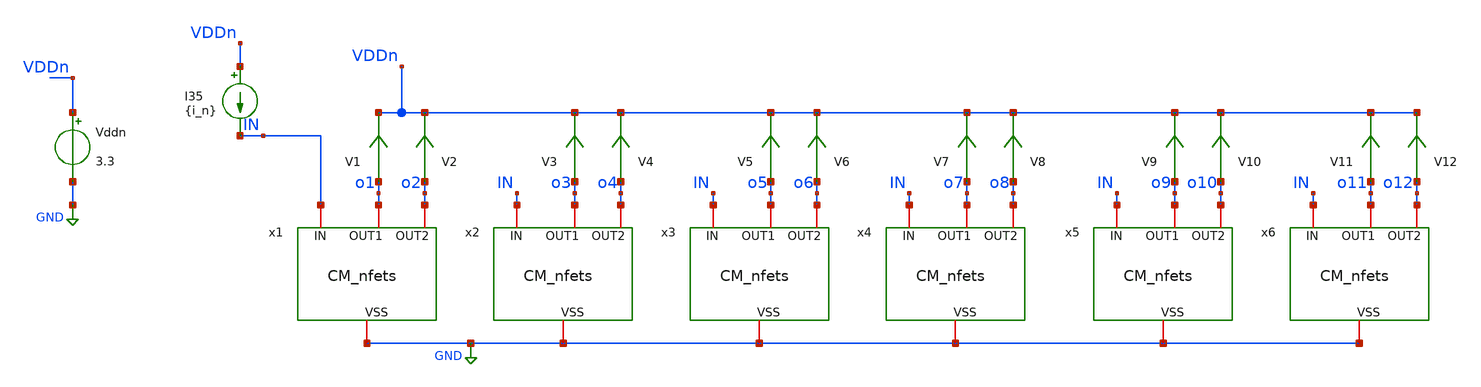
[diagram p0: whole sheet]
** sch_path: TIA_Filter/CurrentMirrors/TB_CM.sch
**.subckt TB_CM
I35 VDDn IN {i_n}
Vddn VDDn GND 3.3
V1 o1 VDDn 0
.save i(v1)
V2 o2 VDDn 0
.save i(v2)
V3 o3 VDDn 0
.save i(v3)
V4 o4 VDDn 0
.save i(v4)
V5 o5 VDDn 0
.save i(v5)
V6 o6 VDDn 0
.save i(v6)
V7 o7 VDDn 0
.save i(v7)
V8 o8 VDDn 0
.save i(v8)
V9 o9 VDDn 0
.save i(v9)
V10 o10 VDDn 0
.save i(v10)
V11 o11 VDDn 0
.save i(v11)
V12 o12 VDDn 0
.save i(v12)
x1 IN o1 o2 GND CM_nfets
x2 IN o3 o4 GND CM_nfets
x3 IN o5 o6 GND CM_nfets
x4 IN o7 o8 GND CM_nfets
x5 IN o9 o10 GND CM_nfets
x6 IN o11 o12 GND CM_nfets
**** begin user architecture code

.include $::180MCU_MODELS/design.ngspice
.lib $::180MCU_MODELS/sm141064.ngspice typical
*.param sw_stat_mismatch=1
*.param sw_stat_global=1

*.include /home/gmaranhao/Desktop/Bracolin/TIA_Filter/CurrentMirrors/layout/spice/CM_nfets_pex4.spice

*.subckt CM_nfets VSS OUT1 OUT2 IN

*Xdut 0 o1 o2 IN CM_nfets
*Xdut2 0 o3 o4 IN CM_nfets
*Xdut3 0 o5 o6 IN CM_nfets
*Xdut4 0 o7 o8 IN CM_nfets
*Xdut5 0 o9 o10 IN CM_nfets
*Xdut6 0 o11 o12 IN CM_nfets




.option gmin=1e-26
.option abstol=1e-18
.option retol=1e-15

.param i_n=1n

.control
save all

let sample_num = 0

*while sample_num<151

reset
op
remzerovec
write TB_CM.raw
*wrdata /home/gmaranhao/Desktop/Bracolin/TIA_Filter/CurrentMirrors/out_cm.txt i(V1) i(V2) i(V3)
*+ i(V4) i(V5) i(V6) i(V7) i(V8) i(V9) i(V
10) i(V11) i(V12)
set appendwrite

*let sample_num = sample_num + 1
*end


.endc
.save all


**** end user architecture code
**.ends

* expanding   symbol:  CurrentMirrors/CM_nfets.sym # of pins=4
** sym_path: TIA_Filter/CurrentMirrors/CM_nfets.sym
** sch_path: TIA_Filter/CurrentMirrors/CM_nfets.sch
.subckt CM_nfets IN OUT1 OUT2 VSS
*.iopin IN
*.iopin OUT1
*.iopin OUT2
*.iopin VSS
XM2[1] IN IN VSS VSS nfet_03v3 L=2u W=2u nf=1 ad='int((nf+1)/2) * W/nf * 0.18u' as='int((nf+2)/2) * W/nf * 0.18u'
+ pd='2*int((nf+1)/2) * (W/nf + 0.18u)' ps='2*int((nf+2)/2) * (W/nf + 0.18u)' nrd='0.18u / W' nrs='0.18u / W'
+ sa=0 sb=0 sd=0 m=1
XM2[2] IN IN VSS VSS nfet_03v3 L=2u W=2u nf=1 ad='int((nf+1)/2) * W/nf * 0.18u' as='int((nf+2)/2) * W/nf * 0.18u'
+ pd='2*int((nf+1)/2) * (W/nf + 0.18u)' ps='2*int((nf+2)/2) * (W/nf + 0.18u)' nrd='0.18u / W' nrs='0.18u / W'
+ sa=0 sb=0 sd=0 m=1
XM2[3] IN IN VSS VSS nfet_03v3 L=2u W=2u nf=1 ad='int((nf+1)/2) * W/nf * 0.18u' as='int((nf+2)/2) * W/nf * 0.18u'
+ pd='2*int((nf+1)/2) * (W/nf + 0.18u)' ps='2*int((nf+2)/2) * (W/nf + 0.18u)' nrd='0.18u / W' nrs='0.18u / W'
+ sa=0 sb=0 sd=0 m=1
XM2[4] IN IN VSS VSS nfet_03v3 L=2u W=2u nf=1 ad='int((nf+1)/2) * W/nf * 0.18u' as='int((nf+2)/2) * W/nf * 0.18u'
+ pd='2*int((nf+1)/2) * (W/nf + 0.18u)' ps='2*int((nf+2)/2) * (W/nf + 0.18u)' nrd='0.18u / W' nrs='0.18u / W'
+ sa=0 sb=0 sd=0 m=1
XM2[5] IN IN VSS VSS nfet_03v3 L=2u W=2u nf=1 ad='int((nf+1)/2) * W/nf * 0.18u' as='int((nf+2)/2) * W/nf * 0.18u'
+ pd='2*int((nf+1)/2) * (W/nf + 0.18u)' ps='2*int((nf+2)/2) * (W/nf + 0.18u)' nrd='0.18u / W' nrs='0.18u / W'
+ sa=0 sb=0 sd=0 m=1
XM2[6] IN IN VSS VSS nfet_03v3 L=2u W=2u nf=1 ad='int((nf+1)/2) * W/nf * 0.18u' as='int((nf+2)/2) * W/nf * 0.18u'
+ pd='2*int((nf+1)/2) * (W/nf + 0.18u)' ps='2*int((nf+2)/2) * (W/nf + 0.18u)' nrd='0.18u / W' nrs='0.18u / W'
+ sa=0 sb=0 sd=0 m=1
XM2 OUT1 IN net3 VSS nfet_03v3 L=2u W=2u nf=1 ad='int((nf+1)/2) * W/nf * 0.18u' as='int((nf+2)/2) * W/nf * 0.18u'
+ pd='2*int((nf+1)/2) * (W/nf + 0.18u)' ps='2*int((nf+2)/2) * (W/nf + 0.18u)' nrd='0.18u / W' nrs='0.18u / W'
+ sa=0 sb=0 sd=0 m=1
XM11 net4 IN net6 VSS nfet_03v3 L=2u W=2u nf=1 ad='int((nf+1)/2) * W/nf * 0.18u' as='int((nf+2)/2) * W/nf * 0.18u'
+ pd='2*int((nf+1)/2) * (W/nf + 0.18u)' ps='2*int((nf+2)/2) * (W/nf + 0.18u)' nrd='0.18u / W' nrs='0.18u / W'
+ sa=0 sb=0 sd=0 m=1
XM12 net6 IN net7 VSS nfet_03v3 L=2u W=2u nf=1 ad='int((nf+1)/2) * W/nf * 0.18u' as='int((nf+2)/2) * W/nf * 0.18u'
+ pd='2*int((nf+1)/2) * (W/nf + 0.18u)' ps='2*int((nf+2)/2) * (W/nf + 0.18u)' nrd='0.18u / W' nrs='0.18u / W'
+ sa=0 sb=0 sd=0 m=1
XM13 net7 IN net8 VSS nfet_03v3 L=2u W=2u nf=1 ad='int((nf+1)/2) * W/nf * 0.18u' as='int((nf+2)/2) * W/nf * 0.18u'
+ pd='2*int((nf+1)/2) * (W/nf + 0.18u)' ps='2*int((nf+2)/2) * (W/nf + 0.18u)' nrd='0.18u / W' nrs='0.18u / W'
+ sa=0 sb=0 sd=0 m=1
XM14 net8 IN net9 VSS nfet_03v3 L=2u W=2u nf=1 ad='int((nf+1)/2) * W/nf * 0.18u' as='int((nf+2)/2) * W/nf * 0.18u'
+ pd='2*int((nf+1)/2) * (W/nf + 0.18u)' ps='2*int((nf+2)/2) * (W/nf + 0.18u)' nrd='0.18u / W' nrs='0.18u / W'
+ sa=0 sb=0 sd=0 m=1
XM15 net9 IN net10 VSS nfet_03v3 L=2u W=2u nf=1 ad='int((nf+1)/2) * W/nf * 0.18u' as='int((nf+2)/2) * W/nf * 0.18u'
+ pd='2*int((nf+1)/2) * (W/nf + 0.18u)' ps='2*int((nf+2)/2) * (W/nf + 0.18u)' nrd='0.18u / W' nrs='0.18u / W'
+ sa=0 sb=0 sd=0 m=1
XM16 net10 IN net11 VSS nfet_03v3 L=2u W=2u nf=1 ad='int((nf+1)/2) * W/nf * 0.18u' as='int((nf+2)/2) * W/nf * 0.18u'
+ pd='2*int((nf+1)/2) * (W/nf + 0.18u)' ps='2*int((nf+2)/2) * (W/nf + 0.18u)' nrd='0.18u / W' nrs='0.18u / W'
+ sa=0 sb=0 sd=0 m=1
XM17 net11 IN net12 VSS nfet_03v3 L=2u W=2u nf=1 ad='int((nf+1)/2) * W/nf * 0.18u' as='int((nf+2)/2) * W/nf * 0.18u'
+ pd='2*int((nf+1)/2) * (W/nf + 0.18u)' ps='2*int((nf+2)/2) * (W/nf + 0.18u)' nrd='0.18u / W' nrs='0.18u / W'
+ sa=0 sb=0 sd=0 m=1
XM18 net12 IN net13 VSS nfet_03v3 L=2u W=2u nf=1 ad='int((nf+1)/2) * W/nf * 0.18u' as='int((nf+2)/2) * W/nf * 0.18u'
+ pd='2*int((nf+1)/2) * (W/nf + 0.18u)' ps='2*int((nf+2)/2) * (W/nf + 0.18u)' nrd='0.18u / W' nrs='0.18u / W'
+ sa=0 sb=0 sd=0 m=1
XM19 net13 IN net14 VSS nfet_03v3 L=2u W=2u nf=1 ad='int((nf+1)/2) * W/nf * 0.18u' as='int((nf+2)/2) * W/nf * 0.18u'
+ pd='2*int((nf+1)/2) * (W/nf + 0.18u)' ps='2*int((nf+2)/2) * (W/nf + 0.18u)' nrd='0.18u / W' nrs='0.18u / W'
+ sa=0 sb=0 sd=0 m=1
XM20 net14 IN net1 VSS nfet_03v3 L=2u W=2u nf=1 ad='int((nf+1)/2) * W/nf * 0.18u' as='int((nf+2)/2) * W/nf * 0.18u'
+ pd='2*int((nf+1)/2) * (W/nf + 0.18u)' ps='2*int((nf+2)/2) * (W/nf + 0.18u)' nrd='0.18u / W' nrs='0.18u / W'
+ sa=0 sb=0 sd=0 m=1
XM21 net1 IN net15 VSS nfet_03v3 L=2u W=2u nf=1 ad='int((nf+1)/2) * W/nf * 0.18u' as='int((nf+2)/2) * W/nf * 0.18u'
+ pd='2*int((nf+1)/2) * (W/nf + 0.18u)' ps='2*int((nf+2)/2) * (W/nf + 0.18u)' nrd='0.18u / W' nrs='0.18u / W'
+ sa=0 sb=0 sd=0 m=1
XM22 net15 IN net16 VSS nfet_03v3 L=2u W=2u nf=1 ad='int((nf+1)/2) * W/nf * 0.18u' as='int((nf+2)/2) * W/nf * 0.18u'
+ pd='2*int((nf+1)/2) * (W/nf + 0.18u)' ps='2*int((nf+2)/2) * (W/nf + 0.18u)' nrd='0.18u / W' nrs='0.18u / W'
+ sa=0 sb=0 sd=0 m=1
XM23 net16 IN net17 VSS nfet_03v3 L=2u W=2u nf=1 ad='int((nf+1)/2) * W/nf * 0.18u' as='int((nf+2)/2) * W/nf * 0.18u'
+ pd='2*int((nf+1)/2) * (W/nf + 0.18u)' ps='2*int((nf+2)/2) * (W/nf + 0.18u)' nrd='0.18u / W' nrs='0.18u / W'
+ sa=0 sb=0 sd=0 m=1
XM24 net17 IN net18 VSS nfet_03v3 L=2u W=2u nf=1 ad='int((nf+1)/2) * W/nf * 0.18u' as='int((nf+2)/2) * W/nf * 0.18u'
+ pd='2*int((nf+1)/2) * (W/nf + 0.18u)' ps='2*int((nf+2)/2) * (W/nf + 0.18u)' nrd='0.18u / W' nrs='0.18u / W'
+ sa=0 sb=0 sd=0 m=1
XM25 net18 IN net19 VSS nfet_03v3 L=2u W=2u nf=1 ad='int((nf+1)/2) * W/nf * 0.18u' as='int((nf+2)/2) * W/nf * 0.18u'
+ pd='2*int((nf+1)/2) * (W/nf + 0.18u)' ps='2*int((nf+2)/2) * (W/nf + 0.18u)' nrd='0.18u / W' nrs='0.18u / W'
+ sa=0 sb=0 sd=0 m=1
XM26 net19 IN net20 VSS nfet_03v3 L=2u W=2u nf=1 ad='int((nf+1)/2) * W/nf * 0.18u' as='int((nf+2)/2) * W/nf * 0.18u'
+ pd='2*int((nf+1)/2) * (W/nf + 0.18u)' ps='2*int((nf+2)/2) * (W/nf + 0.18u)' nrd='0.18u / W' nrs='0.18u / W'
+ sa=0 sb=0 sd=0 m=1
XM27 net20 IN net21 VSS nfet_03v3 L=2u W=2u nf=1 ad='int((nf+1)/2) * W/nf * 0.18u' as='int((nf+2)/2) * W/nf * 0.18u'
+ pd='2*int((nf+1)/2) * (W/nf + 0.18u)' ps='2*int((nf+2)/2) * (W/nf + 0.18u)' nrd='0.18u / W' nrs='0.18u / W'
+ sa=0 sb=0 sd=0 m=1
XM28 net21 IN net22 VSS nfet_03v3 L=2u W=2u nf=1 ad='int((nf+1)/2) * W/nf * 0.18u' as='int((nf+2)/2) * W/nf * 0.18u'
+ pd='2*int((nf+1)/2) * (W/nf + 0.18u)' ps='2*int((nf+2)/2) * (W/nf + 0.18u)' nrd='0.18u / W' nrs='0.18u / W'
+ sa=0 sb=0 sd=0 m=1
XM29 net22 IN net23 VSS nfet_03v3 L=2u W=2u nf=1 ad='int((nf+1)/2) * W/nf * 0.18u' as='int((nf+2)/2) * W/nf * 0.18u'
+ pd='2*int((nf+1)/2) * (W/nf + 0.18u)' ps='2*int((nf+2)/2) * (W/nf + 0.18u)' nrd='0.18u / W' nrs='0.18u / W'
+ sa=0 sb=0 sd=0 m=1
XM30 net23 IN net2 VSS nfet_03v3 L=2u W=2u nf=1 ad='int((nf+1)/2) * W/nf * 0.18u' as='int((nf+2)/2) * W/nf * 0.18u'
+ pd='2*int((nf+1)/2) * (W/nf + 0.18u)' ps='2*int((nf+2)/2) * (W/nf + 0.18u)' nrd='0.18u / W' nrs='0.18u / W'
+ sa=0 sb=0 sd=0 m=1
XM31 net2 IN net24 VSS nfet_03v3 L=2u W=2u nf=1 ad='int((nf+1)/2) * W/nf * 0.18u' as='int((nf+2)/2) * W/nf * 0.18u'
+ pd='2*int((nf+1)/2) * (W/nf + 0.18u)' ps='2*int((nf+2)/2) * (W/nf + 0.18u)' nrd='0.18u / W' nrs='0.18u / W'
+ sa=0 sb=0 sd=0 m=1
XM32 net24 IN net25 VSS nfet_03v3 L=2u W=2u nf=1 ad='int((nf+1)/2) * W/nf * 0.18u' as='int((nf+2)/2) * W/nf * 0.18u'
+ pd='2*int((nf+1)/2) * (W/nf + 0.18u)' ps='2*int((nf+2)/2) * (W/nf + 0.18u)' nrd='0.18u / W' nrs='0.18u / W'
+ sa=0 sb=0 sd=0 m=1
XM33 net25 IN net26 VSS nfet_03v3 L=2u W=2u nf=1 ad='int((nf+1)/2) * W/nf * 0.18u' as='int((nf+2)/2) * W/nf * 0.18u'
+ pd='2*int((nf+1)/2) * (W/nf + 0.18u)' ps='2*int((nf+2)/2) * (W/nf + 0.18u)' nrd='0.18u / W' nrs='0.18u / W'
+ sa=0 sb=0 sd=0 m=1
XM34 net26 IN net27 VSS nfet_03v3 L=2u W=2u nf=1 ad='int((nf+1)/2) * W/nf * 0.18u' as='int((nf+2)/2) * W/nf * 0.18u'
+ pd='2*int((nf+1)/2) * (W/nf + 0.18u)' ps='2*int((nf+2)/2) * (W/nf + 0.18u)' nrd='0.18u / W' nrs='0.18u / W'
+ sa=0 sb=0 sd=0 m=1
XM35 net27 IN net28 VSS nfet_03v3 L=2u W=2u nf=1 ad='int((nf+1)/2) * W/nf * 0.18u' as='int((nf+2)/2) * W/nf * 0.18u'
+ pd='2*int((nf+1)/2) * (W/nf + 0.18u)' ps='2*int((nf+2)/2) * (W/nf + 0.18u)' nrd='0.18u / W' nrs='0.18u / W'
+ sa=0 sb=0 sd=0 m=1
XM36 net28 IN net29 VSS nfet_03v3 L=2u W=2u nf=1 ad='int((nf+1)/2) * W/nf * 0.18u' as='int((nf+2)/2) * W/nf * 0.18u'
+ pd='2*int((nf+1)/2) * (W/nf + 0.18u)' ps='2*int((nf+2)/2) * (W/nf + 0.18u)' nrd='0.18u / W' nrs='0.18u / W'
+ sa=0 sb=0 sd=0 m=1
XM1 net29 IN net30 VSS nfet_03v3 L=2u W=2u nf=1 ad='int((nf+1)/2) * W/nf * 0.18u' as='int((nf+2)/2) * W/nf * 0.18u'
+ pd='2*int((nf+1)/2) * (W/nf + 0.18u)' ps='2*int((nf+2)/2) * (W/nf + 0.18u)' nrd='0.18u / W' nrs='0.18u / W'
+ sa=0 sb=0 sd=0 m=1
XM37 net30 IN net31 VSS nfet_03v3 L=2u W=2u nf=1 ad='int((nf+1)/2) * W/nf * 0.18u' as='int((nf+2)/2) * W/nf * 0.18u'
+ pd='2*int((nf+1)/2) * (W/nf + 0.18u)' ps='2*int((nf+2)/2) * (W/nf + 0.18u)' nrd='0.18u / W' nrs='0.18u / W'
+ sa=0 sb=0 sd=0 m=1
XM38 net31 IN net32 VSS nfet_03v3 L=2u W=2u nf=1 ad='int((nf+1)/2) * W/nf * 0.18u' as='int((nf+2)/2) * W/nf * 0.18u'
+ pd='2*int((nf+1)/2) * (W/nf + 0.18u)' ps='2*int((nf+2)/2) * (W/nf + 0.18u)' nrd='0.18u / W' nrs='0.18u / W'
+ sa=0 sb=0 sd=0 m=1
XM9 net32 IN VSS VSS nfet_03v3 L=2u W=2u nf=1 ad='int((nf+1)/2) * W/nf * 0.18u' as='int((nf+2)/2) * W/nf * 0.18u'
+ pd='2*int((nf+1)/2) * (W/nf + 0.18u)' ps='2*int((nf+2)/2) * (W/nf + 0.18u)' nrd='0.18u / W' nrs='0.18u / W'
+ sa=0 sb=0 sd=0 m=1
XM5 net3 IN net4 VSS nfet_03v3 L=2u W=2u nf=1 ad='int((nf+1)/2) * W/nf * 0.18u' as='int((nf+2)/2) * W/nf * 0.18u'
+ pd='2*int((nf+1)/2) * (W/nf + 0.18u)' ps='2*int((nf+2)/2) * (W/nf + 0.18u)' nrd='0.18u / W' nrs='0.18u / W'
+ sa=0 sb=0 sd=0 m=1
XM8 net5 IN net33 VSS nfet_03v3 L=2u W=2u nf=1 ad='int((nf+1)/2) * W/nf * 0.18u' as='int((nf+2)/2) * W/nf * 0.18u'
+ pd='2*int((nf+1)/2) * (W/nf + 0.18u)' ps='2*int((nf+2)/2) * (W/nf + 0.18u)' nrd='0.18u / W' nrs='0.18u / W'
+ sa=0 sb=0 sd=0 m=1
XM10 net33 IN net34 VSS nfet_03v3 L=2u W=2u nf=1 ad='int((nf+1)/2) * W/nf * 0.18u' as='int((nf+2)/2) * W/nf * 0.18u'
+ pd='2*int((nf+1)/2) * (W/nf + 0.18u)' ps='2*int((nf+2)/2) * (W/nf + 0.18u)' nrd='0.18u / W' nrs='0.18u / W'
+ sa=0 sb=0 sd=0 m=1
XM39 net34 IN net35 VSS nfet_03v3 L=2u W=2u nf=1 ad='int((nf+1)/2) * W/nf * 0.18u' as='int((nf+2)/2) * W/nf * 0.18u'
+ pd='2*int((nf+1)/2) * (W/nf + 0.18u)' ps='2*int((nf+2)/2) * (W/nf + 0.18u)' nrd='0.18u / W' nrs='0.18u / W'
+ sa=0 sb=0 sd=0 m=1
XM40 net35 IN net36 VSS nfet_03v3 L=2u W=2u nf=1 ad='int((nf+1)/2) * W/nf * 0.18u' as='int((nf+2)/2) * W/nf * 0.18u'
+ pd='2*int((nf+1)/2) * (W/nf + 0.18u)' ps='2*int((nf+2)/2) * (W/nf + 0.18u)' nrd='0.18u / W' nrs='0.18u / W'
+ sa=0 sb=0 sd=0 m=1
XM41 net36 IN net37 VSS nfet_03v3 L=2u W=2u nf=1 ad='int((nf+1)/2) * W/nf * 0.18u' as='int((nf+2)/2) * W/nf * 0.18u'
+ pd='2*int((nf+1)/2) * (W/nf + 0.18u)' ps='2*int((nf+2)/2) * (W/nf + 0.18u)' nrd='0.18u / W' nrs='0.18u / W'
+ sa=0 sb=0 sd=0 m=1
XM42 net37 IN net38 VSS nfet_03v3 L=2u W=2u nf=1 ad='int((nf+1)/2) * W/nf * 0.18u' as='int((nf+2)/2) * W/nf * 0.18u'
+ pd='2*int((nf+1)/2) * (W/nf + 0.18u)' ps='2*int((nf+2)/2) * (W/nf + 0.18u)' nrd='0.18u / W' nrs='0.18u / W'
+ sa=0 sb=0 sd=0 m=1
XM43 net38 IN net39 VSS nfet_03v3 L=2u W=2u nf=1 ad='int((nf+1)/2) * W/nf * 0.18u' as='int((nf+2)/2) * W/nf * 0.18u'
+ pd='2*int((nf+1)/2) * (W/nf + 0.18u)' ps='2*int((nf+2)/2) * (W/nf + 0.18u)' nrd='0.18u / W' nrs='0.18u / W'
+ sa=0 sb=0 sd=0 m=1
XM44 net39 IN net40 VSS nfet_03v3 L=2u W=2u nf=1 ad='int((nf+1)/2) * W/nf * 0.18u' as='int((nf+2)/2) * W/nf * 0.18u'
+ pd='2*int((nf+1)/2) * (W/nf + 0.18u)' ps='2*int((nf+2)/2) * (W/nf + 0.18u)' nrd='0.18u / W' nrs='0.18u / W'
+ sa=0 sb=0 sd=0 m=1
XM45 net40 IN net41 VSS nfet_03v3 L=2u W=2u nf=1 ad='int((nf+1)/2) * W/nf * 0.18u' as='int((nf+2)/2) * W/nf * 0.18u'
+ pd='2*int((nf+1)/2) * (W/nf + 0.18u)' ps='2*int((nf+2)/2) * (W/nf + 0.18u)' nrd='0.18u / W' nrs='0.18u / W'
+ sa=0 sb=0 sd=0 m=1
XM46 net41 IN VSS VSS nfet_03v3 L=2u W=2u nf=1 ad='int((nf+1)/2) * W/nf * 0.18u' as='int((nf+2)/2) * W/nf * 0.18u'
+ pd='2*int((nf+1)/2) * (W/nf + 0.18u)' ps='2*int((nf+2)/2) * (W/nf + 0.18u)' nrd='0.18u / W' nrs='0.18u / W'
+ sa=0 sb=0 sd=0 m=1
XM47 OUT2 IN net42 VSS nfet_03v3 L=2u W=2u nf=1 ad='int((nf+1)/2) * W/nf * 0.18u' as='int((nf+2)/2) * W/nf * 0.18u'
+ pd='2*int((nf+1)/2) * (W/nf + 0.18u)' ps='2*int((nf+2)/2) * (W/nf + 0.18u)' nrd='0.18u / W' nrs='0.18u / W'
+ sa=0 sb=0 sd=0 m=1
XM48 net42 IN net43 VSS nfet_03v3 L=2u W=2u nf=1 ad='int((nf+1)/2) * W/nf * 0.18u' as='int((nf+2)/2) * W/nf * 0.18u'
+ pd='2*int((nf+1)/2) * (W/nf + 0.18u)' ps='2*int((nf+2)/2) * (W/nf + 0.18u)' nrd='0.18u / W' nrs='0.18u / W'
+ sa=0 sb=0 sd=0 m=1
XM49 net43 IN net44 VSS nfet_03v3 L=2u W=2u nf=1 ad='int((nf+1)/2) * W/nf * 0.18u' as='int((nf+2)/2) * W/nf * 0.18u'
+ pd='2*int((nf+1)/2) * (W/nf + 0.18u)' ps='2*int((nf+2)/2) * (W/nf + 0.18u)' nrd='0.18u / W' nrs='0.18u / W'
+ sa=0 sb=0 sd=0 m=1
XM50 net44 IN net45 VSS nfet_03v3 L=2u W=2u nf=1 ad='int((nf+1)/2) * W/nf * 0.18u' as='int((nf+2)/2) * W/nf * 0.18u'
+ pd='2*int((nf+1)/2) * (W/nf + 0.18u)' ps='2*int((nf+2)/2) * (W/nf + 0.18u)' nrd='0.18u / W' nrs='0.18u / W'
+ sa=0 sb=0 sd=0 m=1
XM51 net45 IN net46 VSS nfet_03v3 L=2u W=2u nf=1 ad='int((nf+1)/2) * W/nf * 0.18u' as='int((nf+2)/2) * W/nf * 0.18u'
+ pd='2*int((nf+1)/2) * (W/nf + 0.18u)' ps='2*int((nf+2)/2) * (W/nf + 0.18u)' nrd='0.18u / W' nrs='0.18u / W'
+ sa=0 sb=0 sd=0 m=1
XM52 net46 IN net5 VSS nfet_03v3 L=2u W=2u nf=1 ad='int((nf+1)/2) * W/nf * 0.18u' as='int((nf+2)/2) * W/nf * 0.18u'
+ pd='2*int((nf+1)/2) * (W/nf + 0.18u)' ps='2*int((nf+2)/2) * (W/nf + 0.18u)' nrd='0.18u / W' nrs='0.18u / W'
+ sa=0 sb=0 sd=0 m=1
XM1[1] VSS VSS VSS VSS nfet_03v3 L=2u W=2u nf=1 ad='int((nf+1)/2) * W/nf * 0.18u' as='int((nf+2)/2) * W/nf * 0.18u'
+ pd='2*int((nf+1)/2) * (W/nf + 0.18u)' ps='2*int((nf+2)/2) * (W/nf + 0.18u)' nrd='0.18u / W' nrs='0.18u / W'
+ sa=0 sb=0 sd=0 m=1
XM1[2] VSS VSS VSS VSS nfet_03v3 L=2u W=2u nf=1 ad='int((nf+1)/2) * W/nf * 0.18u' as='int((nf+2)/2) * W/nf * 0.18u'
+ pd='2*int((nf+1)/2) * (W/nf + 0.18u)' ps='2*int((nf+2)/2) * (W/nf + 0.18u)' nrd='0.18u / W' nrs='0.18u / W'
+ sa=0 sb=0 sd=0 m=1
XM1[3] VSS VSS VSS VSS nfet_03v3 L=2u W=2u nf=1 ad='int((nf+1)/2) * W/nf * 0.18u' as='int((nf+2)/2) * W/nf * 0.18u'
+ pd='2*int((nf+1)/2) * (W/nf + 0.18u)' ps='2*int((nf+2)/2) * (W/nf + 0.18u)' nrd='0.18u / W' nrs='0.18u / W'
+ sa=0 sb=0 sd=0 m=1
XM1[4] VSS VSS VSS VSS nfet_03v3 L=2u W=2u nf=1 ad='int((nf+1)/2) * W/nf * 0.18u' as='int((nf+2)/2) * W/nf * 0.18u'
+ pd='2*int((nf+1)/2) * (W/nf + 0.18u)' ps='2*int((nf+2)/2) * (W/nf + 0.18u)' nrd='0.18u / W' nrs='0.18u / W'
+ sa=0 sb=0 sd=0 m=1
XM1[5] VSS VSS VSS VSS nfet_03v3 L=2u W=2u nf=1 ad='int((nf+1)/2) * W/nf * 0.18u' as='int((nf+2)/2) * W/nf * 0.18u'
+ pd='2*int((nf+1)/2) * (W/nf + 0.18u)' ps='2*int((nf+2)/2) * (W/nf + 0.18u)' nrd='0.18u / W' nrs='0.18u / W'
+ sa=0 sb=0 sd=0 m=1
XM1[6] VSS VSS VSS VSS nfet_03v3 L=2u W=2u nf=1 ad='int((nf+1)/2) * W/nf * 0.18u' as='int((nf+2)/2) * W/nf * 0.18u'
+ pd='2*int((nf+1)/2) * (W/nf + 0.18u)' ps='2*int((nf+2)/2) * (W/nf + 0.18u)' nrd='0.18u / W' nrs='0.18u / W'
+ sa=0 sb=0 sd=0 m=1
XM1[7] VSS VSS VSS VSS nfet_03v3 L=2u W=2u nf=1 ad='int((nf+1)/2) * W/nf * 0.18u' as='int((nf+2)/2) * W/nf * 0.18u'
+ pd='2*int((nf+1)/2) * (W/nf + 0.18u)' ps='2*int((nf+2)/2) * (W/nf + 0.18u)' nrd='0.18u / W' nrs='0.18u / W'
+ sa=0 sb=0 sd=0 m=1
XM1[8] VSS VSS VSS VSS nfet_03v3 L=2u W=2u nf=1 ad='int((nf+1)/2) * W/nf * 0.18u' as='int((nf+2)/2) * W/nf * 0.18u'
+ pd='2*int((nf+1)/2) * (W/nf + 0.18u)' ps='2*int((nf+2)/2) * (W/nf + 0.18u)' nrd='0.18u / W' nrs='0.18u / W'
+ sa=0 sb=0 sd=0 m=1
XM1[9] VSS VSS VSS VSS nfet_03v3 L=2u W=2u nf=1 ad='int((nf+1)/2) * W/nf * 0.18u' as='int((nf+2)/2) * W/nf * 0.18u'
+ pd='2*int((nf+1)/2) * (W/nf + 0.18u)' ps='2*int((nf+2)/2) * (W/nf + 0.18u)' nrd='0.18u / W' nrs='0.18u / W'
+ sa=0 sb=0 sd=0 m=1
XM1[10] VSS VSS VSS VSS nfet_03v3 L=2u W=2u nf=1 ad='int((nf+1)/2) * W/nf * 0.18u' as='int((nf+2)/2) * W/nf * 0.18u'
+ pd='2*int((nf+1)/2) * (W/nf + 0.18u)' ps='2*int((nf+2)/2) * (W/nf + 0.18u)' nrd='0.18u / W' nrs='0.18u / W'
+ sa=0 sb=0 sd=0 m=1
XM1[11] VSS VSS VSS VSS nfet_03v3 L=2u W=2u nf=1 ad='int((nf+1)/2) * W/nf * 0.18u' as='int((nf+2)/2) * W/nf * 0.18u'
+ pd='2*int((nf+1)/2) * (W/nf + 0.18u)' ps='2*int((nf+2)/2) * (W/nf + 0.18u)' nrd='0.18u / W' nrs='0.18u / W'
+ sa=0 sb=0 sd=0 m=1
XM1[12] VSS VSS VSS VSS nfet_03v3 L=2u W=2u nf=1 ad='int((nf+1)/2) * W/nf * 0.18u' as='int((nf+2)/2) * W/nf * 0.18u'
+ pd='2*int((nf+1)/2) * (W/nf + 0.18u)' ps='2*int((nf+2)/2) * (W/nf + 0.18u)' nrd='0.18u / W' nrs='0.18u / W'
+ sa=0 sb=0 sd=0 m=1
XM1[13] VSS VSS VSS VSS nfet_03v3 L=2u W=2u nf=1 ad='int((nf+1)/2) * W/nf * 0.18u' as='int((nf+2)/2) * W/nf * 0.18u'
+ pd='2*int((nf+1)/2) * (W/nf + 0.18u)' ps='2*int((nf+2)/2) * (W/nf + 0.18u)' nrd='0.18u / W' nrs='0.18u / W'
+ sa=0 sb=0 sd=0 m=1
XM1[14] VSS VSS VSS VSS nfet_03v3 L=2u W=2u nf=1 ad='int((nf+1)/2) * W/nf * 0.18u' as='int((nf+2)/2) * W/nf * 0.18u'
+ pd='2*int((nf+1)/2) * (W/nf + 0.18u)' ps='2*int((nf+2)/2) * (W/nf + 0.18u)' nrd='0.18u / W' nrs='0.18u / W'
+ sa=0 sb=0 sd=0 m=1
XM1[15] VSS VSS VSS VSS nfet_03v3 L=2u W=2u nf=1 ad='int((nf+1)/2) * W/nf * 0.18u' as='int((nf+2)/2) * W/nf * 0.18u'
+ pd='2*int((nf+1)/2) * (W/nf + 0.18u)' ps='2*int((nf+2)/2) * (W/nf + 0.18u)' nrd='0.18u / W' nrs='0.18u / W'
+ sa=0 sb=0 sd=0 m=1
XM1[16] VSS VSS VSS VSS nfet_03v3 L=2u W=2u nf=1 ad='int((nf+1)/2) * W/nf * 0.18u' as='int((nf+2)/2) * W/nf * 0.18u'
+ pd='2*int((nf+1)/2) * (W/nf + 0.18u)' ps='2*int((nf+2)/2) * (W/nf + 0.18u)' nrd='0.18u / W' nrs='0.18u / W'
+ sa=0 sb=0 sd=0 m=1
XM1[17] VSS VSS VSS VSS nfet_03v3 L=2u W=2u nf=1 ad='int((nf+1)/2) * W/nf * 0.18u' as='int((nf+2)/2) * W/nf * 0.18u'
+ pd='2*int((nf+1)/2) * (W/nf + 0.18u)' ps='2*int((nf+2)/2) * (W/nf + 0.18u)' nrd='0.18u / W' nrs='0.18u / W'
+ sa=0 sb=0 sd=0 m=1
XM1[18] VSS VSS VSS VSS nfet_03v3 L=2u W=2u nf=1 ad='int((nf+1)/2) * W/nf * 0.18u' as='int((nf+2)/2) * W/nf * 0.18u'
+ pd='2*int((nf+1)/2) * (W/nf + 0.18u)' ps='2*int((nf+2)/2) * (W/nf + 0.18u)' nrd='0.18u / W' nrs='0.18u / W'
+ sa=0 sb=0 sd=0 m=1
XM1[19] VSS VSS VSS VSS nfet_03v3 L=2u W=2u nf=1 ad='int((nf+1)/2) * W/nf * 0.18u' as='int((nf+2)/2) * W/nf * 0.18u'
+ pd='2*int((nf+1)/2) * (W/nf + 0.18u)' ps='2*int((nf+2)/2) * (W/nf + 0.18u)' nrd='0.18u / W' nrs='0.18u / W'
+ sa=0 sb=0 sd=0 m=1
XM1[20] VSS VSS VSS VSS nfet_03v3 L=2u W=2u nf=1 ad='int((nf+1)/2) * W/nf * 0.18u' as='int((nf+2)/2) * W/nf * 0.18u'
+ pd='2*int((nf+1)/2) * (W/nf + 0.18u)' ps='2*int((nf+2)/2) * (W/nf + 0.18u)' nrd='0.18u / W' nrs='0.18u / W'
+ sa=0 sb=0 sd=0 m=1
XM1[21] VSS VSS VSS VSS nfet_03v3 L=2u W=2u nf=1 ad='int((nf+1)/2) * W/nf * 0.18u' as='int((nf+2)/2) * W/nf * 0.18u'
+ pd='2*int((nf+1)/2) * (W/nf + 0.18u)' ps='2*int((nf+2)/2) * (W/nf + 0.18u)' nrd='0.18u / W' nrs='0.18u / W'
+ sa=0 sb=0 sd=0 m=1
XM1[22] VSS VSS VSS VSS nfet_03v3 L=2u W=2u nf=1 ad='int((nf+1)/2) * W/nf * 0.18u' as='int((nf+2)/2) * W/nf * 0.18u'
+ pd='2*int((nf+1)/2) * (W/nf + 0.18u)' ps='2*int((nf+2)/2) * (W/nf + 0.18u)' nrd='0.18u / W' nrs='0.18u / W'
+ sa=0 sb=0 sd=0 m=1
XM1[23] VSS VSS VSS VSS nfet_03v3 L=2u W=2u nf=1 ad='int((nf+1)/2) * W/nf * 0.18u' as='int((nf+2)/2) * W/nf * 0.18u'
+ pd='2*int((nf+1)/2) * (W/nf + 0.18u)' ps='2*int((nf+2)/2) * (W/nf + 0.18u)' nrd='0.18u / W' nrs='0.18u / W'
+ sa=0 sb=0 sd=0 m=1
XM1[24] VSS VSS VSS VSS nfet_03v3 L=2u W=2u nf=1 ad='int((nf+1)/2) * W/nf * 0.18u' as='int((nf+2)/2) * W/nf * 0.18u'
+ pd='2*int((nf+1)/2) * (W/nf + 0.18u)' ps='2*int((nf+2)/2) * (W/nf + 0.18u)' nrd='0.18u / W' nrs='0.18u / W'
+ sa=0 sb=0 sd=0 m=1
XM1[25] VSS VSS VSS VSS nfet_03v3 L=2u W=2u nf=1 ad='int((nf+1)/2) * W/nf * 0.18u' as='int((nf+2)/2) * W/nf * 0.18u'
+ pd='2*int((nf+1)/2) * (W/nf + 0.18u)' ps='2*int((nf+2)/2) * (W/nf + 0.18u)' nrd='0.18u / W' nrs='0.18u / W'
+ sa=0 sb=0 sd=0 m=1
XM1[26] VSS VSS VSS VSS nfet_03v3 L=2u W=2u nf=1 ad='int((nf+1)/2) * W/nf * 0.18u' as='int((nf+2)/2) * W/nf * 0.18u'
+ pd='2*int((nf+1)/2) * (W/nf + 0.18u)' ps='2*int((nf+2)/2) * (W/nf + 0.18u)' nrd='0.18u / W' nrs='0.18u / W'
+ sa=0 sb=0 sd=0 m=1
XM1[27] VSS VSS VSS VSS nfet_03v3 L=2u W=2u nf=1 ad='int((nf+1)/2) * W/nf * 0.18u' as='int((nf+2)/2) * W/nf * 0.18u'
+ pd='2*int((nf+1)/2) * (W/nf + 0.18u)' ps='2*int((nf+2)/2) * (W/nf + 0.18u)' nrd='0.18u / W' nrs='0.18u / W'
+ sa=0 sb=0 sd=0 m=1
XM1[28] VSS VSS VSS VSS nfet_03v3 L=2u W=2u nf=1 ad='int((nf+1)/2) * W/nf * 0.18u' as='int((nf+2)/2) * W/nf * 0.18u'
+ pd='2*int((nf+1)/2) * (W/nf + 0.18u)' ps='2*int((nf+2)/2) * (W/nf + 0.18u)' nrd='0.18u / W' nrs='0.18u / W'
+ sa=0 sb=0 sd=0 m=1
XM1[29] VSS VSS VSS VSS nfet_03v3 L=2u W=2u nf=1 ad='int((nf+1)/2) * W/nf * 0.18u' as='int((nf+2)/2) * W/nf * 0.18u'
+ pd='2*int((nf+1)/2) * (W/nf + 0.18u)' ps='2*int((nf+2)/2) * (W/nf + 0.18u)' nrd='0.18u / W' nrs='0.18u / W'
+ sa=0 sb=0 sd=0 m=1
XM1[30] VSS VSS VSS VSS nfet_03v3 L=2u W=2u nf=1 ad='int((nf+1)/2) * W/nf * 0.18u' as='int((nf+2)/2) * W/nf * 0.18u'
+ pd='2*int((nf+1)/2) * (W/nf + 0.18u)' ps='2*int((nf+2)/2) * (W/nf + 0.18u)' nrd='0.18u / W' nrs='0.18u / W'
+ sa=0 sb=0 sd=0 m=1
XM1[31] VSS VSS VSS VSS nfet_03v3 L=2u W=2u nf=1 ad='int((nf+1)/2) * W/nf * 0.18u' as='int((nf+2)/2) * W/nf * 0.18u'
+ pd='2*int((nf+1)/2) * (W/nf + 0.18u)' ps='2*int((nf+2)/2) * (W/nf + 0.18u)' nrd='0.18u / W' nrs='0.18u / W'
+ sa=0 sb=0 sd=0 m=1
XM1[32] VSS VSS VSS VSS nfet_03v3 L=2u W=2u nf=1 ad='int((nf+1)/2) * W/nf * 0.18u' as='int((nf+2)/2) * W/nf * 0.18u'
+ pd='2*int((nf+1)/2) * (W/nf + 0.18u)' ps='2*int((nf+2)/2) * (W/nf + 0.18u)' nrd='0.18u / W' nrs='0.18u / W'
+ sa=0 sb=0 sd=0 m=1
XM1[33] VSS VSS VSS VSS nfet_03v3 L=2u W=2u nf=1 ad='int((nf+1)/2) * W/nf * 0.18u' as='int((nf+2)/2) * W/nf * 0.18u'
+ pd='2*int((nf+1)/2) * (W/nf + 0.18u)' ps='2*int((nf+2)/2) * (W/nf + 0.18u)' nrd='0.18u / W' nrs='0.18u / W'
+ sa=0 sb=0 sd=0 m=1
XM1[34] VSS VSS VSS VSS nfet_03v3 L=2u W=2u nf=1 ad='int((nf+1)/2) * W/nf * 0.18u' as='int((nf+2)/2) * W/nf * 0.18u'
+ pd='2*int((nf+1)/2) * (W/nf + 0.18u)' ps='2*int((nf+2)/2) * (W/nf + 0.18u)' nrd='0.18u / W' nrs='0.18u / W'
+ sa=0 sb=0 sd=0 m=1
.ends

.GLOBAL GND
.end
